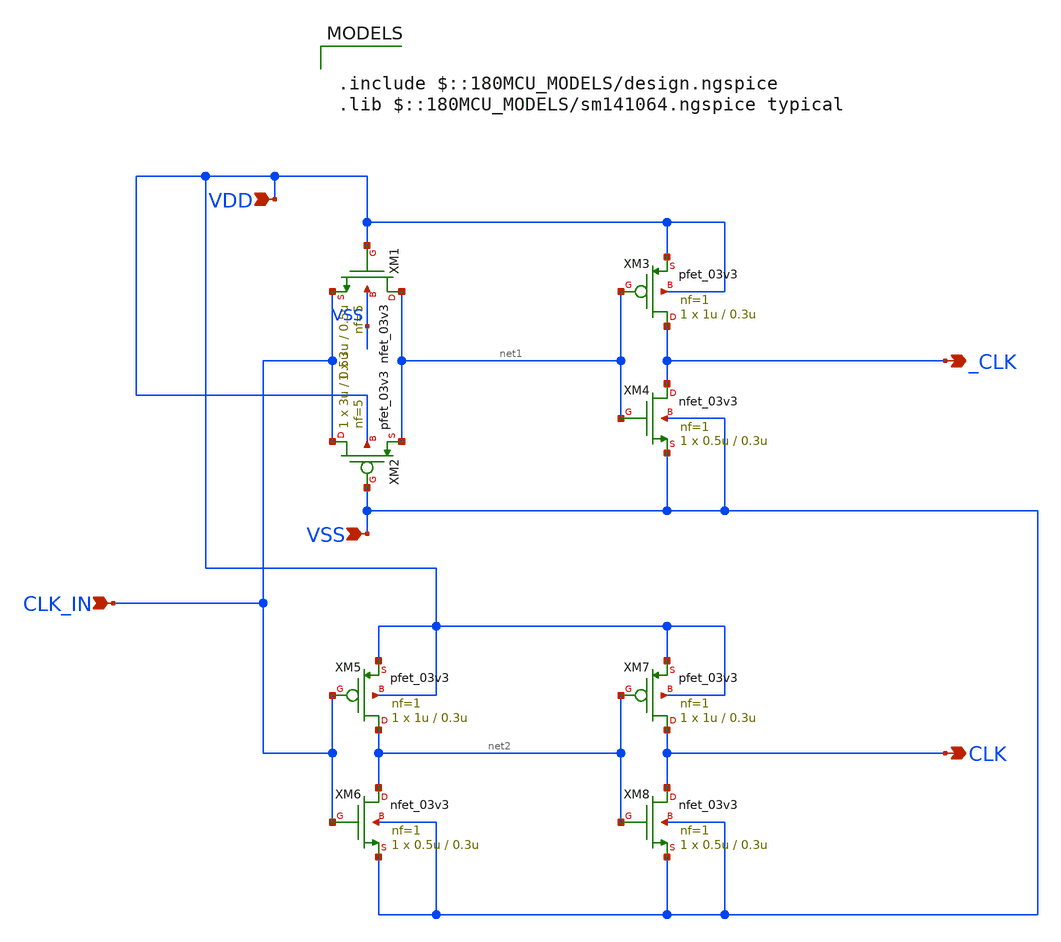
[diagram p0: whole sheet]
** sch_path: Schematics & Results/Chopper Switch/Schematic Files/Complementary_CLK_CS/clk.sch
**.subckt clk CLK _CLK VSS VDD CLK_IN
*.opin CLK
*.opin _CLK
*.ipin VSS
*.ipin VDD
*.ipin CLK_IN
XM1 net1 VDD CLK_IN VSS nfet_03v3 L=0.5u W=3u nf=5 ad='int((nf+1)/2) * W/nf * 0.18u' as='int((nf+2)/2) * W/nf * 0.18u'
+ pd='2*int((nf+1)/2) * (W/nf + 0.18u)' ps='2*int((nf+2)/2) * (W/nf + 0.18u)' nrd='0.18u / W' nrs='0.18u / W'
+ sa=0 sb=0 sd=0 m=1
XM2 CLK_IN VSS net1 VDD pfet_03v3 L=0.5u W=3u nf=5 ad='int((nf+1)/2) * W/nf * 0.18u' as='int((nf+2)/2) * W/nf * 0.18u'
+ pd='2*int((nf+1)/2) * (W/nf + 0.18u)' ps='2*int((nf+2)/2) * (W/nf + 0.18u)' nrd='0.18u / W' nrs='0.18u / W'
+ sa=0 sb=0 sd=0 m=1
XM3 _CLK net1 VDD VDD pfet_03v3 L=0.3u W=1u nf=1 ad='int((nf+1)/2) * W/nf * 0.18u' as='int((nf+2)/2) * W/nf * 0.18u'
+ pd='2*int((nf+1)/2) * (W/nf + 0.18u)' ps='2*int((nf+2)/2) * (W/nf + 0.18u)' nrd='0.18u / W' nrs='0.18u / W'
+ sa=0 sb=0 sd=0 m=1
XM4 _CLK net1 VSS VSS nfet_03v3 L=0.3u W=0.5u nf=1 ad='int((nf+1)/2) * W/nf * 0.18u' as='int((nf+2)/2) * W/nf * 0.18u'
+ pd='2*int((nf+1)/2) * (W/nf + 0.18u)' ps='2*int((nf+2)/2) * (W/nf + 0.18u)' nrd='0.18u / W' nrs='0.18u / W'
+ sa=0 sb=0 sd=0 m=1
XM5 net2 CLK_IN VDD VDD pfet_03v3 L=0.3u W=1u nf=1 ad='int((nf+1)/2) * W/nf * 0.18u' as='int((nf+2)/2) * W/nf * 0.18u'
+ pd='2*int((nf+1)/2) * (W/nf + 0.18u)' ps='2*int((nf+2)/2) * (W/nf + 0.18u)' nrd='0.18u / W' nrs='0.18u / W'
+ sa=0 sb=0 sd=0 m=1
XM6 net2 CLK_IN VSS VSS nfet_03v3 L=0.3u W=0.5u nf=1 ad='int((nf+1)/2) * W/nf * 0.18u' as='int((nf+2)/2) * W/nf * 0.18u'
+ pd='2*int((nf+1)/2) * (W/nf + 0.18u)' ps='2*int((nf+2)/2) * (W/nf + 0.18u)' nrd='0.18u / W' nrs='0.18u / W'
+ sa=0 sb=0 sd=0 m=1
XM7 CLK net2 VDD VDD pfet_03v3 L=0.3u W=1u nf=1 ad='int((nf+1)/2) * W/nf * 0.18u' as='int((nf+2)/2) * W/nf * 0.18u'
+ pd='2*int((nf+1)/2) * (W/nf + 0.18u)' ps='2*int((nf+2)/2) * (W/nf + 0.18u)' nrd='0.18u / W' nrs='0.18u / W'
+ sa=0 sb=0 sd=0 m=1
XM8 CLK net2 VSS VSS nfet_03v3 L=0.3u W=0.5u nf=1 ad='int((nf+1)/2) * W/nf * 0.18u' as='int((nf+2)/2) * W/nf * 0.18u'
+ pd='2*int((nf+1)/2) * (W/nf + 0.18u)' ps='2*int((nf+2)/2) * (W/nf + 0.18u)' nrd='0.18u / W' nrs='0.18u / W'
+ sa=0 sb=0 sd=0 m=1
**** begin user architecture code

.include $::180MCU_MODELS/design.ngspice
.lib $::180MCU_MODELS/sm141064.ngspice typical

**** end user architecture code
**.ends
.end
